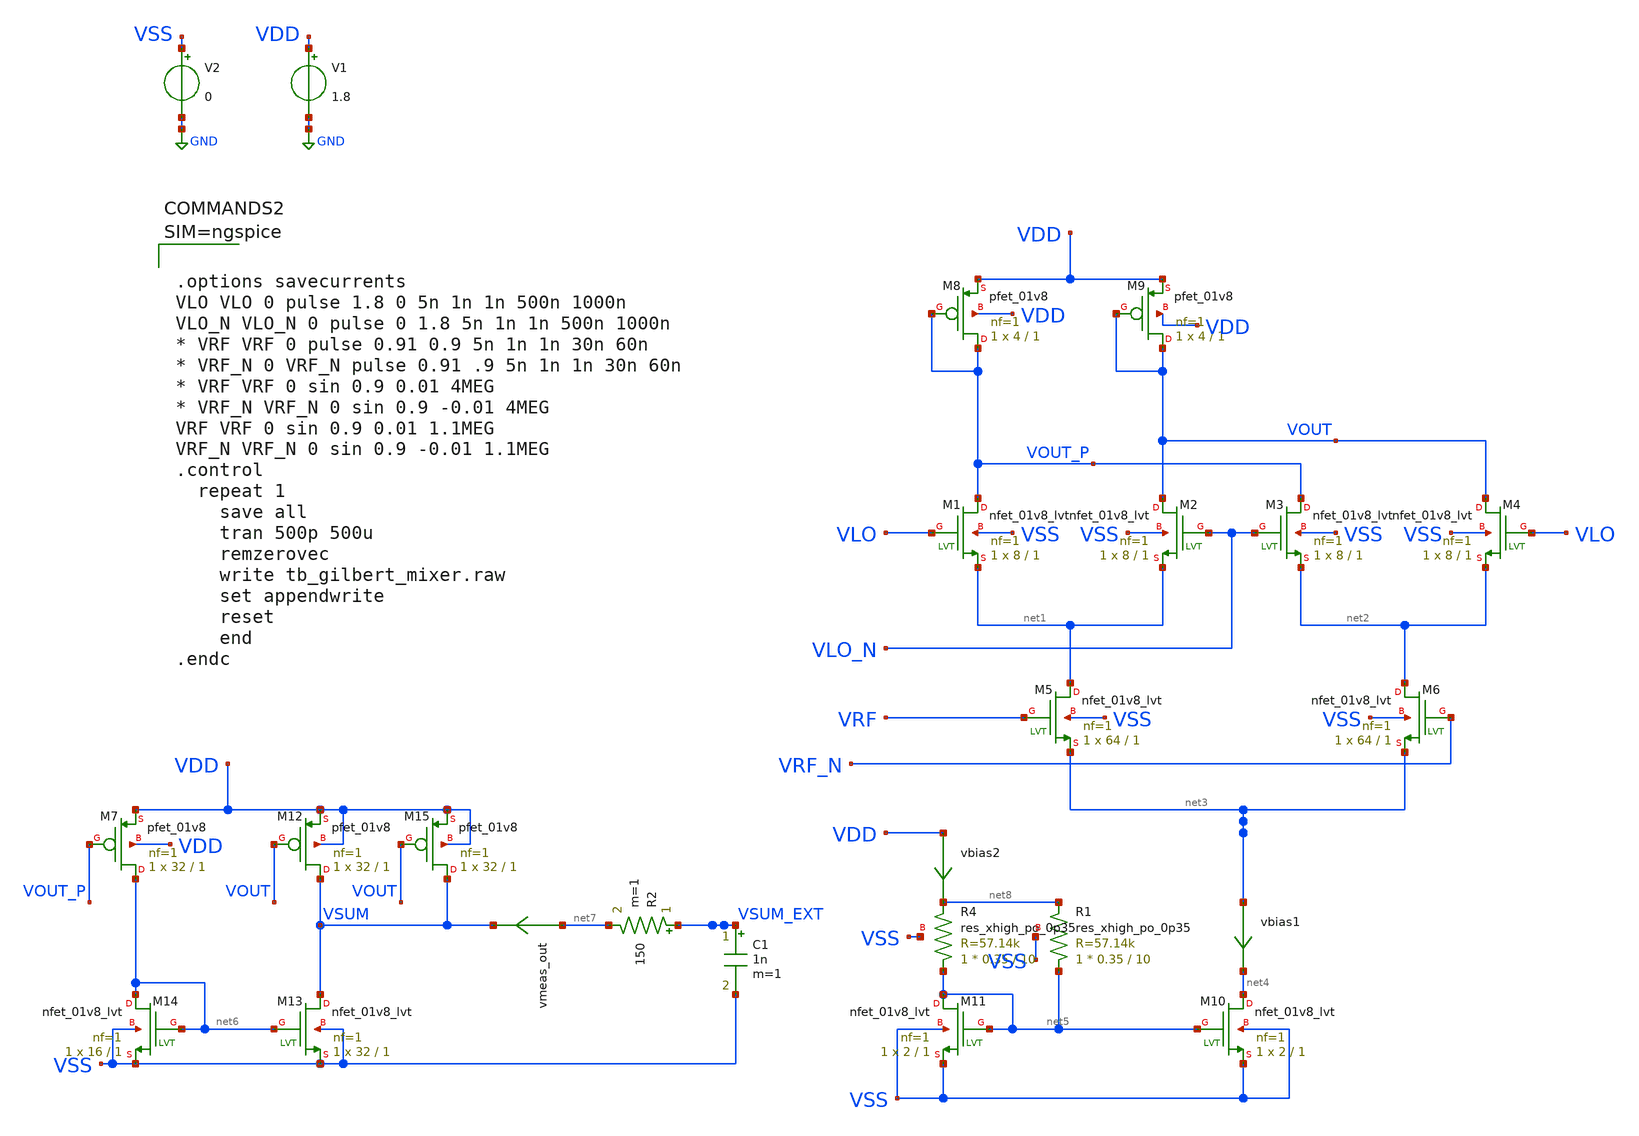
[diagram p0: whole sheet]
** sch_path: xschem/tb_gilbert_mixer.sch
**.subckt tb_gilbert_mixer
XM1 VOUT_P VLO net1 VSS sky130_fd_pr__nfet_01v8_lvt L=1 W=8 nf=1 ad='int((nf+1)/2) * W/nf * 0.29' as='int((nf+2)/2) * W/nf * 0.29'
+ pd='2*int((nf+1)/2) * (W/nf + 0.29)' ps='2*int((nf+2)/2) * (W/nf + 0.29)' nrd='0.29 / W' nrs='0.29 / W'
+ sa=0 sb=0 sd=0 mult=1 m=1
XM2 VOUT VLO_N net1 VSS sky130_fd_pr__nfet_01v8_lvt L=1 W=8 nf=1 ad='int((nf+1)/2) * W/nf * 0.29' as='int((nf+2)/2) * W/nf * 0.29'
+ pd='2*int((nf+1)/2) * (W/nf + 0.29)' ps='2*int((nf+2)/2) * (W/nf + 0.29)' nrd='0.29 / W' nrs='0.29 / W'
+ sa=0 sb=0 sd=0 mult=1 m=1
XM3 VOUT_P VLO_N net2 VSS sky130_fd_pr__nfet_01v8_lvt L=1 W=8 nf=1 ad='int((nf+1)/2) * W/nf * 0.29' as='int((nf+2)/2) * W/nf * 0.29'
+ pd='2*int((nf+1)/2) * (W/nf + 0.29)' ps='2*int((nf+2)/2) * (W/nf + 0.29)' nrd='0.29 / W' nrs='0.29 / W'
+ sa=0 sb=0 sd=0 mult=1 m=1
XM4 VOUT VLO net2 VSS sky130_fd_pr__nfet_01v8_lvt L=1 W=8 nf=1 ad='int((nf+1)/2) * W/nf * 0.29' as='int((nf+2)/2) * W/nf * 0.29'
+ pd='2*int((nf+1)/2) * (W/nf + 0.29)' ps='2*int((nf+2)/2) * (W/nf + 0.29)' nrd='0.29 / W' nrs='0.29 / W'
+ sa=0 sb=0 sd=0 mult=1 m=1
XM5 net1 VRF net3 VSS sky130_fd_pr__nfet_01v8_lvt L=1 W=64 nf=1 ad='int((nf+1)/2) * W/nf * 0.29' as='int((nf+2)/2) * W/nf * 0.29'
+ pd='2*int((nf+1)/2) * (W/nf + 0.29)' ps='2*int((nf+2)/2) * (W/nf + 0.29)' nrd='0.29 / W' nrs='0.29 / W'
+ sa=0 sb=0 sd=0 mult=1 m=1
XM6 net2 VRF_N net3 VSS sky130_fd_pr__nfet_01v8_lvt L=1 W=64 nf=1 ad='int((nf+1)/2) * W/nf * 0.29' as='int((nf+2)/2) * W/nf * 0.29'
+ pd='2*int((nf+1)/2) * (W/nf + 0.29)' ps='2*int((nf+2)/2) * (W/nf + 0.29)' nrd='0.29 / W' nrs='0.29 / W'
+ sa=0 sb=0 sd=0 mult=1 m=1
XM8 VOUT_P VOUT_P VDD VDD sky130_fd_pr__pfet_01v8 L=1 W=4 nf=1 ad='int((nf+1)/2) * W/nf * 0.29' as='int((nf+2)/2) * W/nf * 0.29'
+ pd='2*int((nf+1)/2) * (W/nf + 0.29)' ps='2*int((nf+2)/2) * (W/nf + 0.29)' nrd='0.29 / W' nrs='0.29 / W'
+ sa=0 sb=0 sd=0 mult=1 m=1
XM9 VOUT VOUT VDD VDD sky130_fd_pr__pfet_01v8 L=1 W=4 nf=1 ad='int((nf+1)/2) * W/nf * 0.29' as='int((nf+2)/2) * W/nf * 0.29'
+ pd='2*int((nf+1)/2) * (W/nf + 0.29)' ps='2*int((nf+2)/2) * (W/nf + 0.29)' nrd='0.29 / W' nrs='0.29 / W'
+ sa=0 sb=0 sd=0 mult=1 m=1
V1 VDD GND 1.8
V2 VSS GND 0
XM10 net4 net5 VSS VSS sky130_fd_pr__nfet_01v8_lvt L=1 W=2 nf=1 ad='int((nf+1)/2) * W/nf * 0.29' as='int((nf+2)/2) * W/nf * 0.29'
+ pd='2*int((nf+1)/2) * (W/nf + 0.29)' ps='2*int((nf+2)/2) * (W/nf + 0.29)' nrd='0.29 / W' nrs='0.29 / W'
+ sa=0 sb=0 sd=0 mult=1 m=1
vbias1 net3 net4 0
.save i(vbias1)
XM11 net5 net5 VSS VSS sky130_fd_pr__nfet_01v8_lvt L=1 W=2 nf=1 ad='int((nf+1)/2) * W/nf * 0.29' as='int((nf+2)/2) * W/nf * 0.29'
+ pd='2*int((nf+1)/2) * (W/nf + 0.29)' ps='2*int((nf+2)/2) * (W/nf + 0.29)' nrd='0.29 / W' nrs='0.29 / W'
+ sa=0 sb=0 sd=0 mult=1 m=1
vbias2 VDD net8 0
.save i(vbias2)
XM7 net6 VOUT_P VDD VDD sky130_fd_pr__pfet_01v8 L=1 W=32 nf=1 ad='int((nf+1)/2) * W/nf * 0.29' as='int((nf+2)/2) * W/nf * 0.29'
+ pd='2*int((nf+1)/2) * (W/nf + 0.29)' ps='2*int((nf+2)/2) * (W/nf + 0.29)' nrd='0.29 / W' nrs='0.29 / W'
+ sa=0 sb=0 sd=0 mult=1 m=1
XM12 VSUM VOUT VDD VDD sky130_fd_pr__pfet_01v8 L=1 W=32 nf=1 ad='int((nf+1)/2) * W/nf * 0.29' as='int((nf+2)/2) * W/nf * 0.29'
+ pd='2*int((nf+1)/2) * (W/nf + 0.29)' ps='2*int((nf+2)/2) * (W/nf + 0.29)' nrd='0.29 / W' nrs='0.29 / W'
+ sa=0 sb=0 sd=0 mult=1 m=1
XM13 VSUM net6 VSS VSS sky130_fd_pr__nfet_01v8_lvt L=1 W=32 nf=1 ad='int((nf+1)/2) * W/nf * 0.29' as='int((nf+2)/2) * W/nf * 0.29'
+ pd='2*int((nf+1)/2) * (W/nf + 0.29)' ps='2*int((nf+2)/2) * (W/nf + 0.29)' nrd='0.29 / W' nrs='0.29 / W'
+ sa=0 sb=0 sd=0 mult=1 m=1
XM14 net6 net6 VSS VSS sky130_fd_pr__nfet_01v8_lvt L=1 W=16 nf=1 ad='int((nf+1)/2) * W/nf * 0.29' as='int((nf+2)/2) * W/nf * 0.29'
+ pd='2*int((nf+1)/2) * (W/nf + 0.29)' ps='2*int((nf+2)/2) * (W/nf + 0.29)' nrd='0.29 / W' nrs='0.29 / W'
+ sa=0 sb=0 sd=0 mult=1 m=1
C1 VSUM_EXT VSS 1n m=1
vmeas_out net7 VSUM 0
.save i(vmeas_out)
R2 VSUM_EXT net7 150 m=1
XR4 net5 net8 VSS sky130_fd_pr__res_xhigh_po_0p35 L=10 mult=1 m=1
XR1 net5 net8 VSS sky130_fd_pr__res_xhigh_po_0p35 L=10 mult=1 m=1
XM15 VSUM VOUT VDD VDD sky130_fd_pr__pfet_01v8 L=1 W=32 nf=1 ad='int((nf+1)/2) * W/nf * 0.29' as='int((nf+2)/2) * W/nf * 0.29'
+ pd='2*int((nf+1)/2) * (W/nf + 0.29)' ps='2*int((nf+2)/2) * (W/nf + 0.29)' nrd='0.29 / W' nrs='0.29 / W'
+ sa=0 sb=0 sd=0 mult=1 m=1
**** begin user architecture code

** opencircuitdesign pdks install
.lib $::SKYWATER_MODELS/sky130.lib.spice tt_mm





.options savecurrents
VLO VLO 0 pulse 1.8 0 5n 1n 1n 500n 1000n
VLO_N VLO_N 0 pulse 0 1.8 5n 1n 1n 500n 1000n
* VRF VRF 0 pulse 0.91 0.9 5n 1n 1n 30n 60n
* VRF_N 0 VRF_N pulse 0.91 .9 5n 1n 1n 30n 60n
* VRF VRF 0 sin 0.9 0.01 4MEG
* VRF_N VRF_N 0 sin 0.9 -0.01 4MEG
VRF VRF 0 sin 0.9 0.01 1.1MEG
VRF_N VRF_N 0 sin 0.9 -0.01 1.1MEG
.control
  repeat 1
    save all
    tran 500p 500u
    remzerovec
    write tb_gilbert_mixer.raw
    set appendwrite
    reset
    end
.endc



**** end user architecture code
**.ends
.GLOBAL GND
.end
